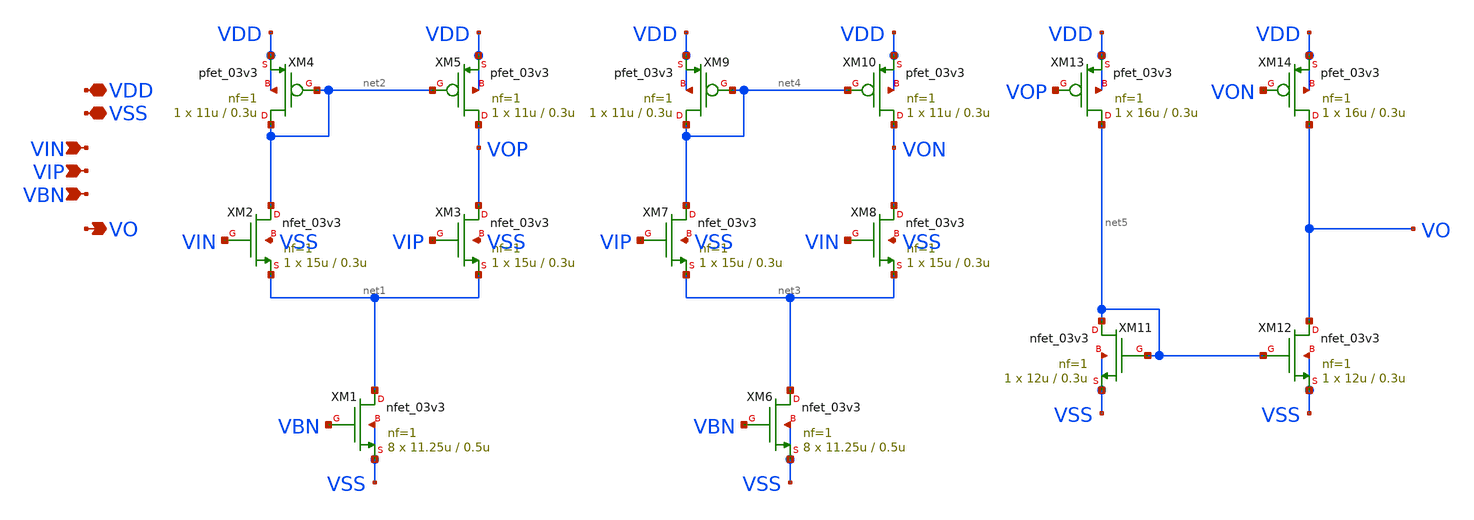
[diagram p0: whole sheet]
** sch_path: designs/libs/core_analog/d2s_converter/d2s_converter.sch
**.subckt d2s_converter VDD VSS VIN VIP VO VBN
*.iopin VDD
*.iopin VSS
*.ipin VIN
*.ipin VIP
*.opin VO
*.ipin VBN
XM2 net2 VIN net1 VSS nfet_03v3 L=0.3u W=15u nf=1 ad='int((nf+1)/2) * W/nf * 0.18u' as='int((nf+2)/2) * W/nf * 0.18u'
+ pd='2*int((nf+1)/2) * (W/nf + 0.18u)' ps='2*int((nf+2)/2) * (W/nf + 0.18u)' nrd='0.18u / W' nrs='0.18u / W'
+ sa=0 sb=0 sd=0 m=1
XM3 VOP VIP net1 VSS nfet_03v3 L=0.3u W=15u nf=1 ad='int((nf+1)/2) * W/nf * 0.18u' as='int((nf+2)/2) * W/nf * 0.18u'
+ pd='2*int((nf+1)/2) * (W/nf + 0.18u)' ps='2*int((nf+2)/2) * (W/nf + 0.18u)' nrd='0.18u / W' nrs='0.18u / W'
+ sa=0 sb=0 sd=0 m=1
XM4 net2 net2 VDD VDD pfet_03v3 L=0.3u W=11u nf=1 ad='int((nf+1)/2) * W/nf * 0.18u' as='int((nf+2)/2) * W/nf * 0.18u'
+ pd='2*int((nf+1)/2) * (W/nf + 0.18u)' ps='2*int((nf+2)/2) * (W/nf + 0.18u)' nrd='0.18u / W' nrs='0.18u / W'
+ sa=0 sb=0 sd=0 m=1
XM5 VOP net2 VDD VDD pfet_03v3 L=0.3u W=11u nf=1 ad='int((nf+1)/2) * W/nf * 0.18u' as='int((nf+2)/2) * W/nf * 0.18u'
+ pd='2*int((nf+1)/2) * (W/nf + 0.18u)' ps='2*int((nf+2)/2) * (W/nf + 0.18u)' nrd='0.18u / W' nrs='0.18u / W'
+ sa=0 sb=0 sd=0 m=1
XM7 net4 VIP net3 VSS nfet_03v3 L=0.3u W=15u nf=1 ad='int((nf+1)/2) * W/nf * 0.18u' as='int((nf+2)/2) * W/nf * 0.18u'
+ pd='2*int((nf+1)/2) * (W/nf + 0.18u)' ps='2*int((nf+2)/2) * (W/nf + 0.18u)' nrd='0.18u / W' nrs='0.18u / W'
+ sa=0 sb=0 sd=0 m=1
XM8 VON VIN net3 VSS nfet_03v3 L=0.3u W=15u nf=1 ad='int((nf+1)/2) * W/nf * 0.18u' as='int((nf+2)/2) * W/nf * 0.18u'
+ pd='2*int((nf+1)/2) * (W/nf + 0.18u)' ps='2*int((nf+2)/2) * (W/nf + 0.18u)' nrd='0.18u / W' nrs='0.18u / W'
+ sa=0 sb=0 sd=0 m=1
XM9 net4 net4 VDD VDD pfet_03v3 L=0.3u W=11u nf=1 ad='int((nf+1)/2) * W/nf * 0.18u' as='int((nf+2)/2) * W/nf * 0.18u'
+ pd='2*int((nf+1)/2) * (W/nf + 0.18u)' ps='2*int((nf+2)/2) * (W/nf + 0.18u)' nrd='0.18u / W' nrs='0.18u / W'
+ sa=0 sb=0 sd=0 m=1
XM10 VON net4 VDD VDD pfet_03v3 L=0.3u W=11u nf=1 ad='int((nf+1)/2) * W/nf * 0.18u' as='int((nf+2)/2) * W/nf * 0.18u'
+ pd='2*int((nf+1)/2) * (W/nf + 0.18u)' ps='2*int((nf+2)/2) * (W/nf + 0.18u)' nrd='0.18u / W' nrs='0.18u / W'
+ sa=0 sb=0 sd=0 m=1
XM11 net5 net5 VSS VSS nfet_03v3 L=0.3u W=12u nf=1 ad='int((nf+1)/2) * W/nf * 0.18u' as='int((nf+2)/2) * W/nf * 0.18u'
+ pd='2*int((nf+1)/2) * (W/nf + 0.18u)' ps='2*int((nf+2)/2) * (W/nf + 0.18u)' nrd='0.18u / W' nrs='0.18u / W'
+ sa=0 sb=0 sd=0 m=1
XM12 VO net5 VSS VSS nfet_03v3 L=0.3u W=12u nf=1 ad='int((nf+1)/2) * W/nf * 0.18u' as='int((nf+2)/2) * W/nf * 0.18u'
+ pd='2*int((nf+1)/2) * (W/nf + 0.18u)' ps='2*int((nf+2)/2) * (W/nf + 0.18u)' nrd='0.18u / W' nrs='0.18u / W'
+ sa=0 sb=0 sd=0 m=1
XM13 net5 VOP VDD VDD pfet_03v3 L=0.3u W=16u nf=1 ad='int((nf+1)/2) * W/nf * 0.18u' as='int((nf+2)/2) * W/nf * 0.18u'
+ pd='2*int((nf+1)/2) * (W/nf + 0.18u)' ps='2*int((nf+2)/2) * (W/nf + 0.18u)' nrd='0.18u / W' nrs='0.18u / W'
+ sa=0 sb=0 sd=0 m=1
XM14 VO VON VDD VDD pfet_03v3 L=0.3u W=16u nf=1 ad='int((nf+1)/2) * W/nf * 0.18u' as='int((nf+2)/2) * W/nf * 0.18u'
+ pd='2*int((nf+1)/2) * (W/nf + 0.18u)' ps='2*int((nf+2)/2) * (W/nf + 0.18u)' nrd='0.18u / W' nrs='0.18u / W'
+ sa=0 sb=0 sd=0 m=1
XM6 net3 VBN VSS VSS nfet_03v3 L=0.5u W=11.25u nf=1 ad='int((nf+1)/2) * W/nf * 0.18u' as='int((nf+2)/2) * W/nf * 0.18u'
+ pd='2*int((nf+1)/2) * (W/nf + 0.18u)' ps='2*int((nf+2)/2) * (W/nf + 0.18u)' nrd='0.18u / W' nrs='0.18u / W'
+ sa=0 sb=0 sd=0 m=8
XM1 net1 VBN VSS VSS nfet_03v3 L=0.5u W=11.25u nf=1 ad='int((nf+1)/2) * W/nf * 0.18u' as='int((nf+2)/2) * W/nf * 0.18u'
+ pd='2*int((nf+1)/2) * (W/nf + 0.18u)' ps='2*int((nf+2)/2) * (W/nf + 0.18u)' nrd='0.18u / W' nrs='0.18u / W'
+ sa=0 sb=0 sd=0 m=8
**.ends
.end
